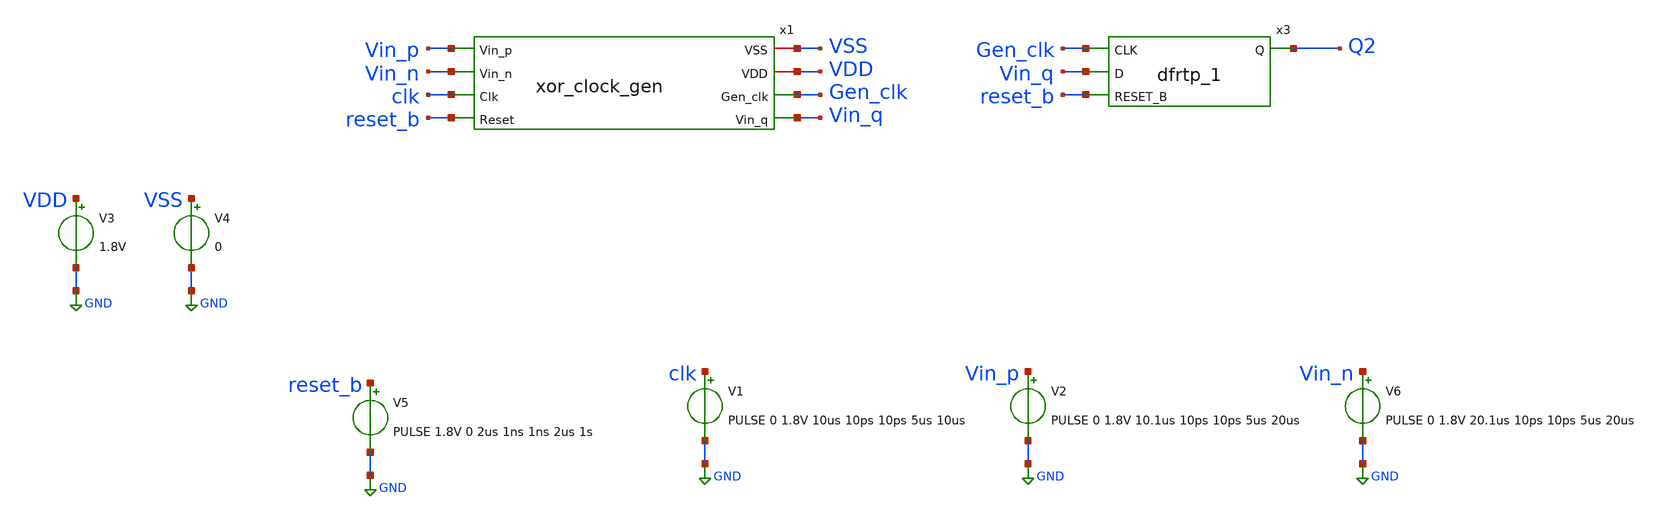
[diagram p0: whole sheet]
** sch_path: xschem/tests/xor_clock_gen/xor_clock_gen_test.sch
**.subckt xor_clock_gen_test
V3 VDD GND 1.8V
V4 VSS GND 0
x1 VSS Vin_p VDD Vin_n Gen_clk clk Vin_q reset_b xor_clock_gen
V5 reset_b GND PULSE 1.8V 0 2us 1ns 1ns 2us 1s
V1 clk GND PULSE 0 1.8V 10us 10ps 10ps 5us 10us
V2 Vin_p GND PULSE 0 1.8V 10.1us 10ps 10ps 5us 20us
V6 Vin_n GND PULSE 0 1.8V 20.1us 10ps 10ps 5us 20us
x3 Gen_clk Vin_q reset_b VSS VSS VDD VDD Q2 sky130_fd_sc_hd__dfrtp_1
**** begin user architecture code
 .lib $::SKYWATER_MODELS/sky130.lib.spice tt
.include $::SKYWATER_STDCELLS/sky130_fd_sc_hd.spice


.options acct list
.temp 25
*vvcc VDD 0 dc 1.8
*vvss VSS 0 0
.control
tran 0.8u 50u
*plot RST_PLS clk+2 Pulse+4
plot Vin_p-Vin_n clk reset_b-2 Gen_clk Vin_q Q2+2
write xor_clock_gen_test.raw
.endc


**** end user architecture code
**.ends
.GLOBAL GND
.end
